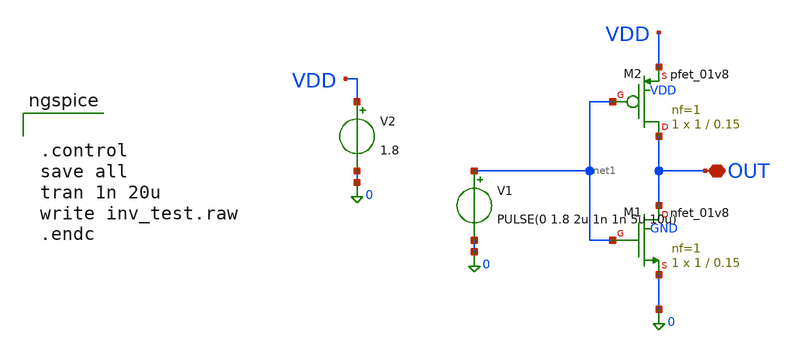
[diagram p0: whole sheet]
** sch_path: design_data/xschem/inv_test.sch
**.subckt inv_test OUT
*.iopin OUT
XM1 OUT net1 0 GND sky130_fd_pr__nfet_01v8 L=0.15 W=1 nf=1 ad='int((1 + 1)/2) * 1 / 1 * 0.29' as='int((1 + 2)/2) * 1 / 1 * 0.29'
+ pd='2*int((1 + 1)/2) * (1 / 1 + 0.29)' ps='2*int((1 + 2)/2) * (1 / 1 + 0.29)' nrd='0.29 / 1 ' nrs='0.29 / 1 '
+ sa=0 sb=0 sd=0 mult=1 m=1
XM2 OUT net1 VDD VDD sky130_fd_pr__pfet_01v8 L=0.15 W=1 nf=1 ad='int((1 + 1)/2) * 1 / 1 * 0.29' as='int((1 + 2)/2) * 1 / 1 * 0.29'
+ pd='2*int((1 + 1)/2) * (1 / 1 + 0.29)' ps='2*int((1 + 2)/2) * (1 / 1 + 0.29)' nrd='0.29 / 1 ' nrs='0.29 / 1 '
+ sa=0 sb=0 sd=0 mult=1 m=1
V1 net1 0 PULSE(0 1.8 2u 1n 1n 5u 10u)
V2 VDD 0 1.8
**** begin user architecture code


.control
save all
tran 1n 20u
write inv_test.raw
.endc



** opencircuitdesign pdks install
.lib $::SKYWATER_MODELS/sky130.lib.spice tt

**** end user architecture code
**.ends
.end
